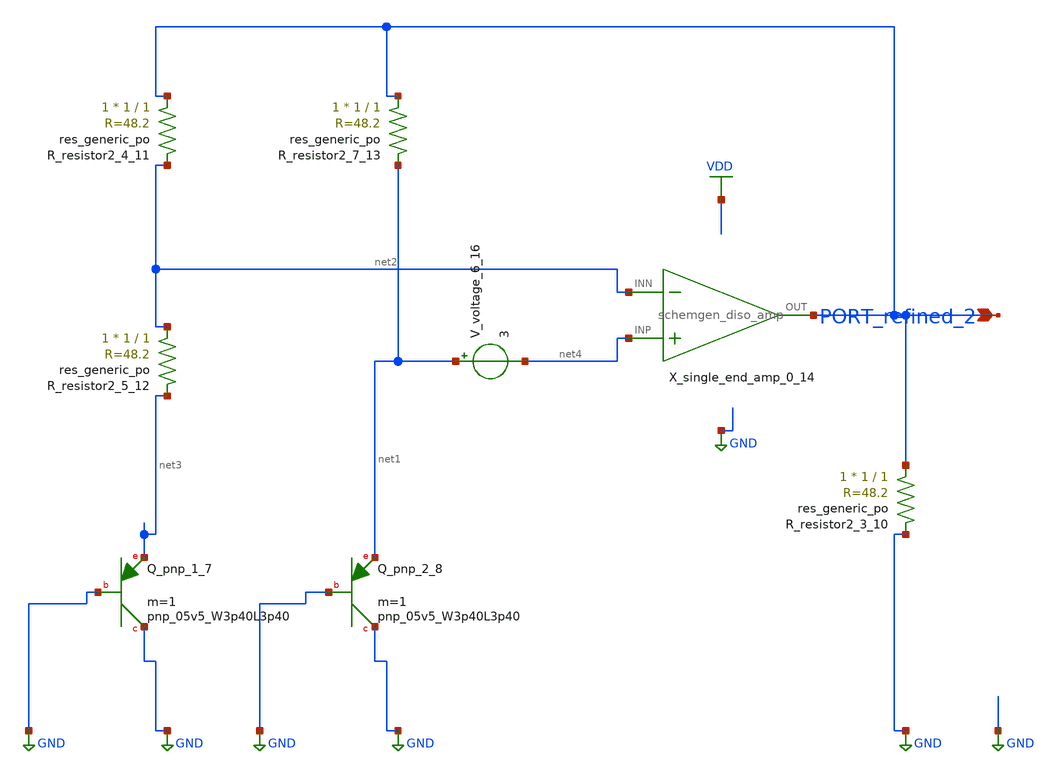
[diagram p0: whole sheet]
** sch_path: schematics/Image2Net/041.sch
**.subckt 041 PORT_refined_2
*.ipin PORT_refined_2
XQ_pnp_1_7 GND GND net3 sky130_fd_pr__pnp_05v5_W3p40L3p40 m=1
XQ_pnp_2_8 GND GND net1 sky130_fd_pr__pnp_05v5_W3p40L3p40 m=1
XR_resistor2_3_10 PORT_refined_2 GND sky130_fd_pr__res_generic_po W=1 L=1 m=1
XR_resistor2_4_11 PORT_refined_2 net2 sky130_fd_pr__res_generic_po W=1 L=1 m=1
XR_resistor2_5_12 net2 net3 sky130_fd_pr__res_generic_po W=1 L=1 m=1
XR_resistor2_7_13 PORT_refined_2 net1 sky130_fd_pr__res_generic_po W=1 L=1 m=1
X_single_end_amp_0_14 net4 net2 PORT_refined_2 schemgen_diso_amp
V_voltage_6_16 net1 net4 3
**.ends

* expanding   symbol:  schemgen_diso_amp.sym # of pins=3
** sym_path: symbols/schemgen_diso_amp.sym
.subckt schemgen_diso_amp INP INN OUT
* SchemGen ideal op-amp: Vout = 1e5 * (V(INP) - V(INN))
E1 OUT 0 INP INN 1e5
.ends schemgen_diso_amp
.GLOBAL GND
.GLOBAL VDD
.end
